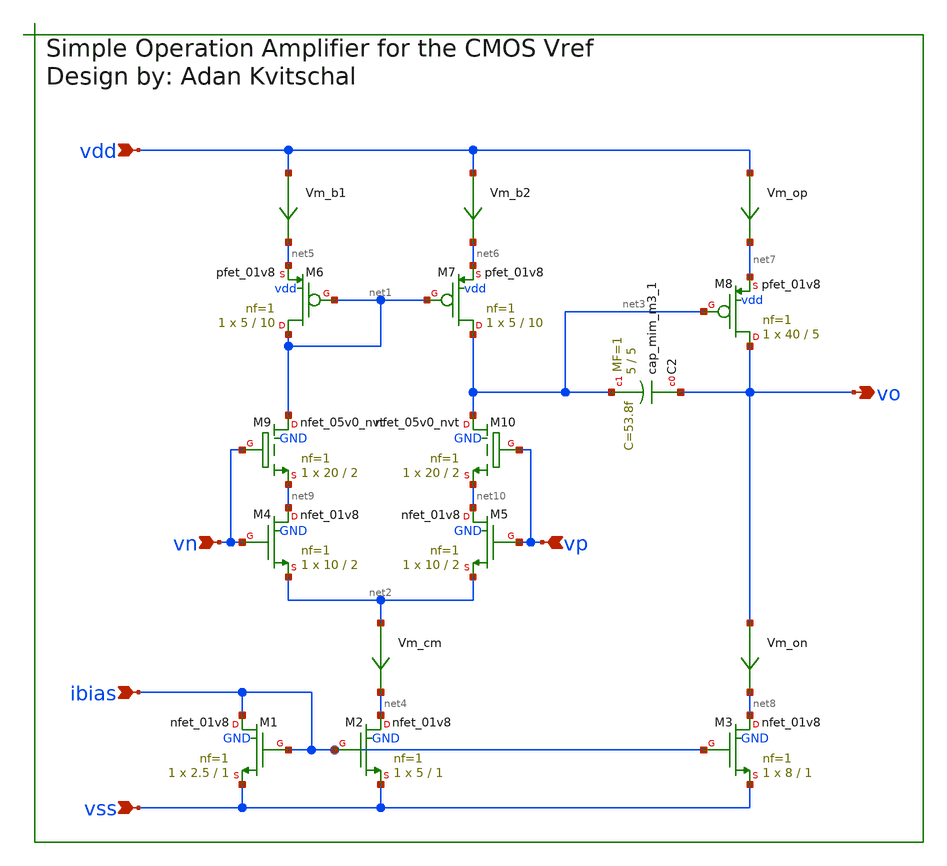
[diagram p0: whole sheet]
** sch_path: xschem/output_amp.sch
**.subckt output_amp vp vn ibias vo vss vdd
*.ipin vp
*.ipin vn
*.ipin ibias
*.opin vo
*.ipin vss
*.ipin vdd
XM1 ibias ibias vss GND sky130_fd_pr__nfet_01v8 L=1 W=2.5 nf=1 ad='int((nf+1)/2) * W/nf * 0.29' as='int((nf+2)/2) * W/nf * 0.29'
+ pd='2*int((nf+1)/2) * (W/nf + 0.29)' ps='2*int((nf+2)/2) * (W/nf + 0.29)' nrd='0.29 / W' nrs='0.29 / W'
+ sa=0 sb=0 sd=0 mult=1 m=1
XM2 net4 ibias vss GND sky130_fd_pr__nfet_01v8 L=1 W=5 nf=1 ad='int((nf+1)/2) * W/nf * 0.29' as='int((nf+2)/2) * W/nf * 0.29'
+ pd='2*int((nf+1)/2) * (W/nf + 0.29)' ps='2*int((nf+2)/2) * (W/nf + 0.29)' nrd='0.29 / W' nrs='0.29 / W'
+ sa=0 sb=0 sd=0 mult=1 m=1
XM7 net3 net1 net6 vdd sky130_fd_pr__pfet_01v8 L=10 W=5 nf=1 ad='int((nf+1)/2) * W/nf * 0.29' as='int((nf+2)/2) * W/nf * 0.29'
+ pd='2*int((nf+1)/2) * (W/nf + 0.29)' ps='2*int((nf+2)/2) * (W/nf + 0.29)' nrd='0.29 / W' nrs='0.29 / W'
+ sa=0 sb=0 sd=0 mult=1 m=1
XM4 net9 vn net2 GND sky130_fd_pr__nfet_01v8 L=2 W=10 nf=1 ad='int((nf+1)/2) * W/nf * 0.29' as='int((nf+2)/2) * W/nf * 0.29'
+ pd='2*int((nf+1)/2) * (W/nf + 0.29)' ps='2*int((nf+2)/2) * (W/nf + 0.29)' nrd='0.29 / W' nrs='0.29 / W'
+ sa=0 sb=0 sd=0 mult=1 m=1
XM5 net10 vp net2 GND sky130_fd_pr__nfet_01v8 L=2 W=10 nf=1 ad='int((nf+1)/2) * W/nf * 0.29' as='int((nf+2)/2) * W/nf * 0.29'
+ pd='2*int((nf+1)/2) * (W/nf + 0.29)' ps='2*int((nf+2)/2) * (W/nf + 0.29)' nrd='0.29 / W' nrs='0.29 / W'
+ sa=0 sb=0 sd=0 mult=1 m=1
XM6 net1 net1 net5 vdd sky130_fd_pr__pfet_01v8 L=10 W=5 nf=1 ad='int((nf+1)/2) * W/nf * 0.29' as='int((nf+2)/2) * W/nf * 0.29'
+ pd='2*int((nf+1)/2) * (W/nf + 0.29)' ps='2*int((nf+2)/2) * (W/nf + 0.29)' nrd='0.29 / W' nrs='0.29 / W'
+ sa=0 sb=0 sd=0 mult=1 m=1
Vm_b1 vdd net5 0
.save i(vm_b1)
XM3 net8 ibias vss GND sky130_fd_pr__nfet_01v8 L=1 W=8 nf=1 ad='int((nf+1)/2) * W/nf * 0.29' as='int((nf+2)/2) * W/nf * 0.29'
+ pd='2*int((nf+1)/2) * (W/nf + 0.29)' ps='2*int((nf+2)/2) * (W/nf + 0.29)' nrd='0.29 / W' nrs='0.29 / W'
+ sa=0 sb=0 sd=0 mult=1 m=1
XM8 vo net3 net7 vdd sky130_fd_pr__pfet_01v8 L=5 W=40 nf=1 ad='int((nf+1)/2) * W/nf * 0.29' as='int((nf+2)/2) * W/nf * 0.29'
+ pd='2*int((nf+1)/2) * (W/nf + 0.29)' ps='2*int((nf+2)/2) * (W/nf + 0.29)' nrd='0.29 / W' nrs='0.29 / W'
+ sa=0 sb=0 sd=0 mult=1 m=1
Vm_op vdd net7 0
.save i(vm_op)
Vm_cm net2 net4 0
.save i(vm_cm)
Vm_b2 vdd net6 0
.save i(vm_b2)
XC2 vo net3 sky130_fd_pr__cap_mim_m3_1 W=5 L=5 MF=1 m=1
Vm_on vo net8 0
.save i(vm_on)
XM9 net1 vn net9 GND sky130_fd_pr__nfet_05v0_nvt L=2 W=20 nf=1 ad='int((nf+1)/2) * W/nf * 0.29' as='int((nf+2)/2) * W/nf * 0.29'
+ pd='2*int((nf+1)/2) * (W/nf + 0.29)' ps='2*int((nf+2)/2) * (W/nf + 0.29)' nrd='0.29 / W' nrs='0.29 / W'
+ sa=0 sb=0 sd=0 mult=1 m=1
XM10 net3 vp net10 GND sky130_fd_pr__nfet_05v0_nvt L=2 W=20 nf=1 ad='int((nf+1)/2) * W/nf * 0.29' as='int((nf+2)/2) * W/nf * 0.29'
+ pd='2*int((nf+1)/2) * (W/nf + 0.29)' ps='2*int((nf+2)/2) * (W/nf + 0.29)' nrd='0.29 / W' nrs='0.29 / W'
+ sa=0 sb=0 sd=0 mult=1 m=1
**.ends
.end
